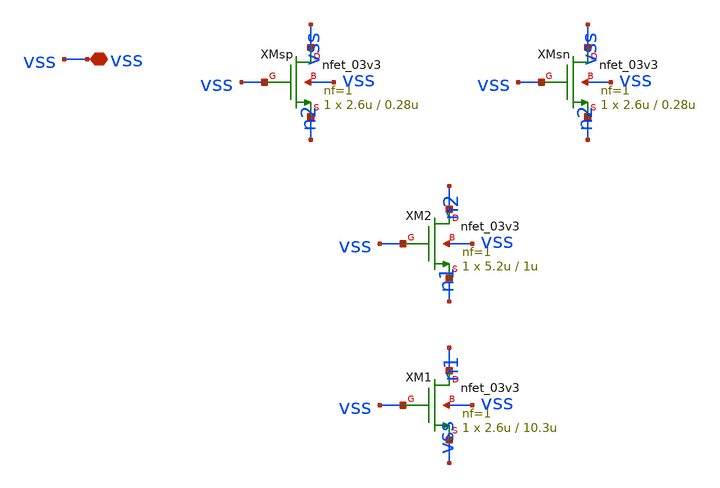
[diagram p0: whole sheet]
** sch_path: design/analog/dummy_cell.sch
**.subckt dummy_cell vss
*.iopin vss
XM1 n1 vss vss vss nfet_03v3 L=10.3u W=2.6u nf=1 ad='int((nf+1)/2) * W/nf * 0.18u' as='int((nf+2)/2) * W/nf * 0.18u'
+ pd='2*int((nf+1)/2) * (W/nf + 0.18u)' ps='2*int((nf+2)/2) * (W/nf + 0.18u)' nrd='0.18u / W' nrs='0.18u / W'
+ sa=0 sb=0 sd=0 m=1
XM2 n2 vss n1 vss nfet_03v3 L=1u W=5.2u nf=1 ad='int((nf+1)/2) * W/nf * 0.18u' as='int((nf+2)/2) * W/nf * 0.18u'
+ pd='2*int((nf+1)/2) * (W/nf + 0.18u)' ps='2*int((nf+2)/2) * (W/nf + 0.18u)' nrd='0.18u / W' nrs='0.18u / W'
+ sa=0 sb=0 sd=0 m=1
XMsp vss vss n2 vss nfet_03v3 L=0.28u W=2.6u nf=1 ad='int((nf+1)/2) * W/nf * 0.18u' as='int((nf+2)/2) * W/nf * 0.18u'
+ pd='2*int((nf+1)/2) * (W/nf + 0.18u)' ps='2*int((nf+2)/2) * (W/nf + 0.18u)' nrd='0.18u / W' nrs='0.18u / W'
+ sa=0 sb=0 sd=0 m=1
XMsn vss vss n2 vss nfet_03v3 L=0.28u W=2.6u nf=1 ad='int((nf+1)/2) * W/nf * 0.18u' as='int((nf+2)/2) * W/nf * 0.18u'
+ pd='2*int((nf+1)/2) * (W/nf + 0.18u)' ps='2*int((nf+2)/2) * (W/nf + 0.18u)' nrd='0.18u / W' nrs='0.18u / W'
+ sa=0 sb=0 sd=0 m=1
**.ends
.end
